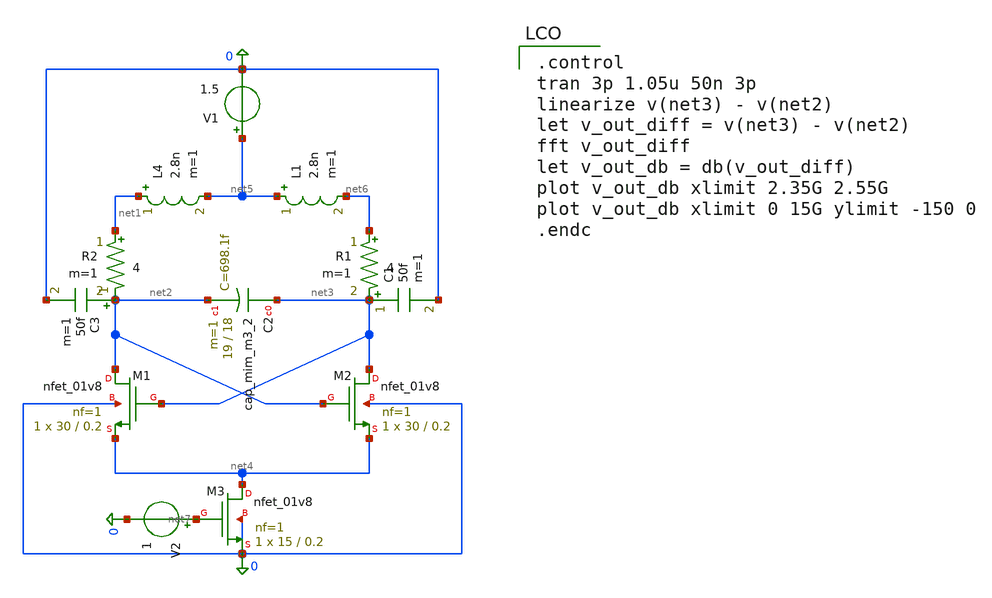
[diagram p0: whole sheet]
** sch_path: schematic/lco.sch
**.subckt lco
L1 net5 net6 2.8n m=1
XC2 net3 net2 sky130_fd_pr__cap_mim_m3_2 W=19 L=18 MF=1 m=1
XM1 net2 net3 net4 0 sky130_fd_pr__nfet_01v8 L=0.2 W=30 nf=1 ad='int((1 + 1)/2) * 30 / 1 * 0.29' as='int((1 + 2)/2) * 30 / 1 * 0.29'
+ pd='2*int((1 + 1)/2) * (30 / 1 + 0.29)' ps='2*int((1 + 2)/2) * (30 / 1 + 0.29)' nrd='0.29 / 30 ' nrs='0.29 / 30 '
+ sa=0 sb=0 sd=0 mult=1 m=1
XM2 net3 net2 net4 0 sky130_fd_pr__nfet_01v8 L=0.2 W=30 nf=1 ad='int((1 + 1)/2) * 30 / 1 * 0.29' as='int((1 + 2)/2) * 30 / 1 * 0.29'
+ pd='2*int((1 + 1)/2) * (30 / 1 + 0.29)' ps='2*int((1 + 2)/2) * (30 / 1 + 0.29)' nrd='0.29 / 30 ' nrs='0.29 / 30 '
+ sa=0 sb=0 sd=0 mult=1 m=1
V1 net5 0 1.5
L4 net1 net5 2.8n m=1
R1 net6 net3 4 m=1
R2 net1 net2 4 m=1
XM3 net4 net7 0 0 sky130_fd_pr__nfet_01v8 L=0.2 W=15 nf=1 ad='int((1 + 1)/2) * 15 / 1 * 0.29' as='int((1 + 2)/2) * 15 / 1 * 0.29'
+ pd='2*int((1 + 1)/2) * (15 / 1 + 0.29)' ps='2*int((1 + 2)/2) * (15 / 1 + 0.29)' nrd='0.29 / 15 ' nrs='0.29 / 15 '
+ sa=0 sb=0 sd=0 mult=1 m=1
V2 net7 0 1
C1 net3 0 50f m=1
C3 net2 0 50f m=1
**** begin user architecture code

.control
tran 3p 1.05u 50n 3p
linearize v(net3) - v(net2)
let v_out_diff = v(net3) - v(net2)
fft v_out_diff
let v_out_db = db(v_out_diff)
plot v_out_db xlimit 2.35G 2.55G
plot v_out_db xlimit 0 15G ylimit -150 0
.endc


** opencircuitdesign pdks install
.lib $::SKYWATER_MODELS/sky130.lib.spice tt

**** end user architecture code
**.ends
.end
